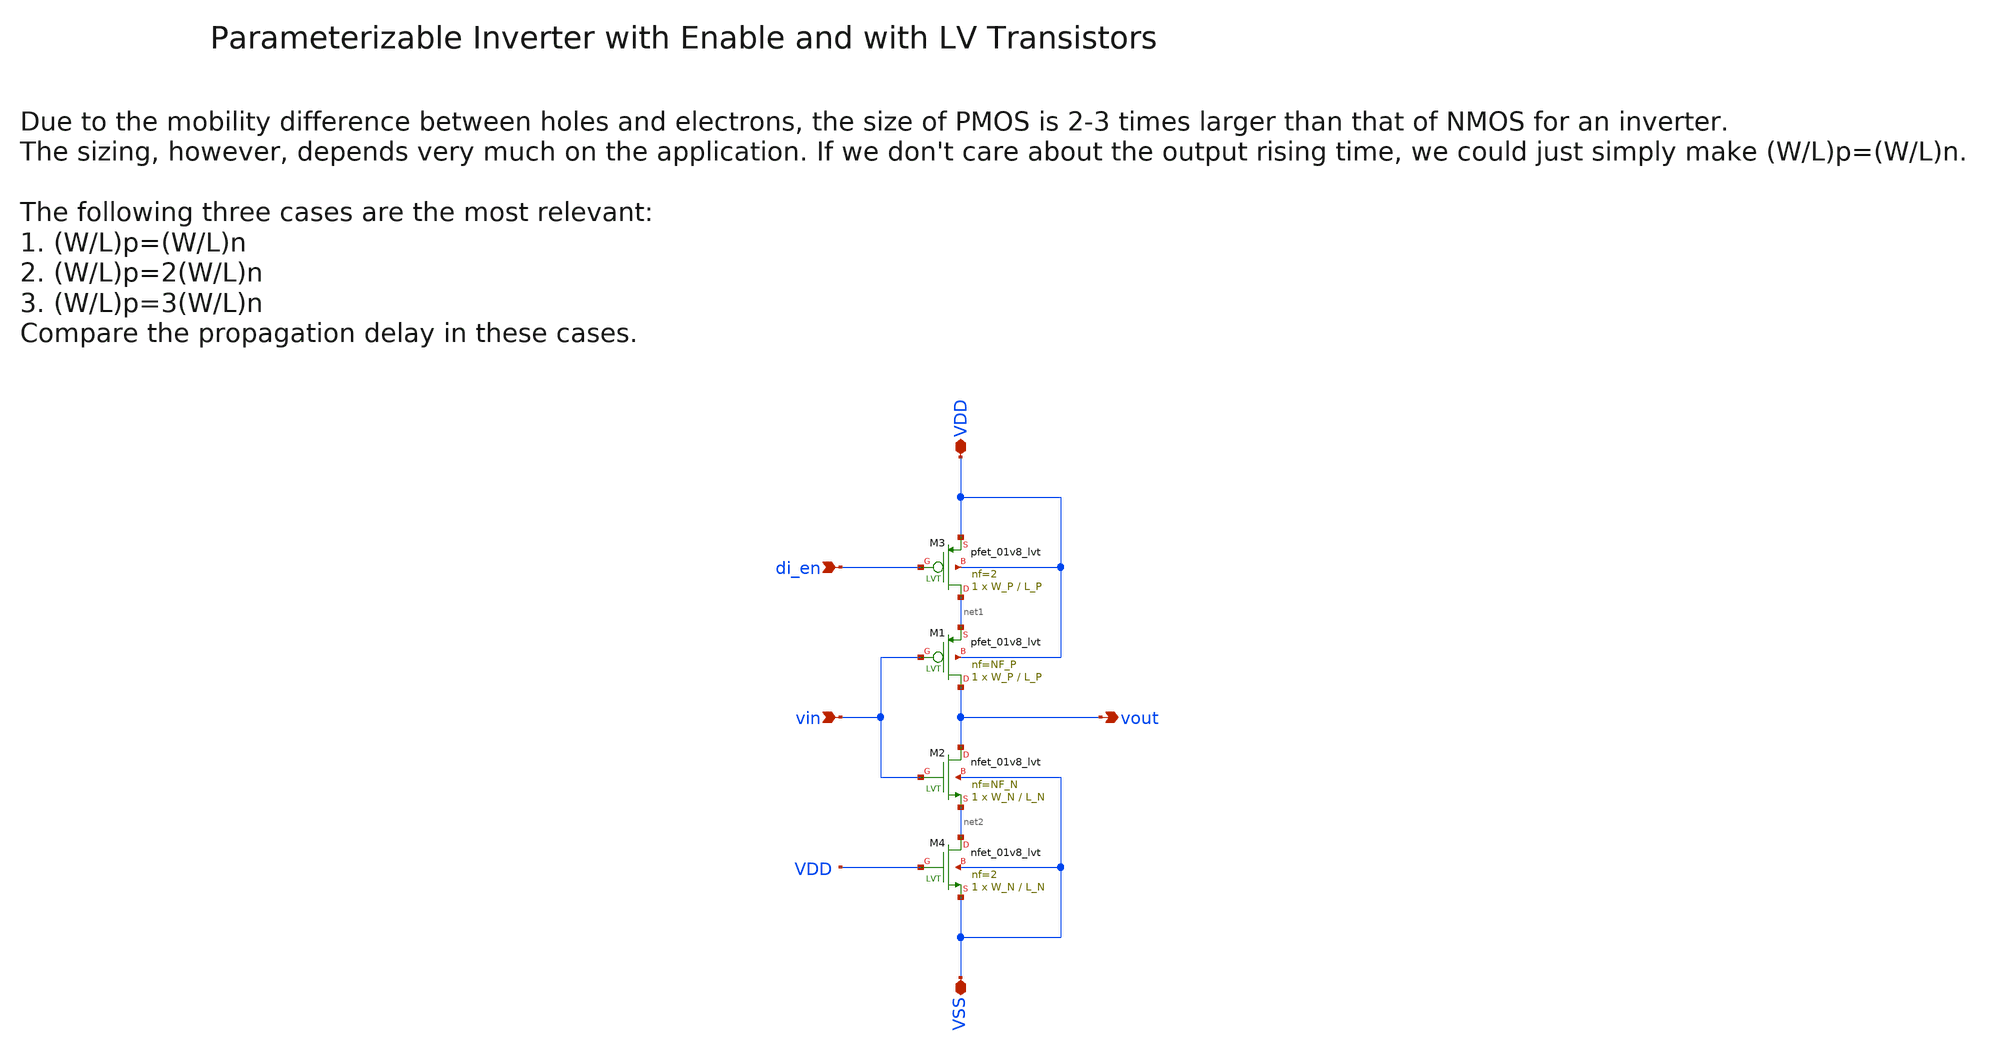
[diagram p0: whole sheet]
** sch_path: sky130/xschem/generic/wspr_tx_iqmod_mfb_lpf_ota_core_inv_lv_en_gen.sch
**.subckt wspr_tx_iqmod_mfb_lpf_ota_core_inv_lv_en_gen vin VDD VSS vout di_en
*.ipin vin
*.iopin VDD
*.iopin VSS
*.opin vout
*.ipin di_en
XM1 vout vin net1 VDD sky130_fd_pr__pfet_01v8_lvt L=L_P W=W_P nf=NF_P ad='int((NF_P + 1)/2) * W_P / NF_P * 0.29'
+ as='int((NF_P + 2)/2) * W_P / NF_P * 0.29' pd='2*int((NF_P + 1)/2) * (W_P / NF_P + 0.29)' ps='2*int((NF_P + 2)/2) * (W_P / NF_P + 0.29)'
+ nrd='0.29 / W_P ' nrs='0.29 / W_P ' sa=0 sb=0 sd=0 mult=1 m=1
XM3 net1 di_en VDD VDD sky130_fd_pr__pfet_01v8_lvt L=L_P W=W_P nf=2 ad='int((2 + 1)/2) * W_P / 2 * 0.29'
+ as='int((2 + 2)/2) * W_P / 2 * 0.29' pd='2*int((2 + 1)/2) * (W_P / 2 + 0.29)' ps='2*int((2 + 2)/2) * (W_P / 2 + 0.29)'
+ nrd='0.29 / W_P ' nrs='0.29 / W_P ' sa=0 sb=0 sd=0 mult=1 m=1
XM2 vout vin net2 VSS sky130_fd_pr__nfet_01v8_lvt L=L_N W=W_N nf=NF_N ad='int((NF_N + 1)/2) * W_N / NF_N * 0.29'
+ as='int((NF_N + 2)/2) * W_N / NF_N * 0.29' pd='2*int((NF_N + 1)/2) * (W_N / NF_N + 0.29)' ps='2*int((NF_N + 2)/2) * (W_N / NF_N + 0.29)'
+ nrd='0.29 / W_N ' nrs='0.29 / W_N ' sa=0 sb=0 sd=0 mult=1 m=1
XM4 net2 VDD VSS VSS sky130_fd_pr__nfet_01v8_lvt L=L_N W=W_N nf=2 ad='int((2 + 1)/2) * W_N / 2 * 0.29'
+ as='int((2 + 2)/2) * W_N / 2 * 0.29' pd='2*int((2 + 1)/2) * (W_N / 2 + 0.29)' ps='2*int((2 + 2)/2) * (W_N / 2 + 0.29)'
+ nrd='0.29 / W_N ' nrs='0.29 / W_N ' sa=0 sb=0 sd=0 mult=1 m=1
**.ends
.end
